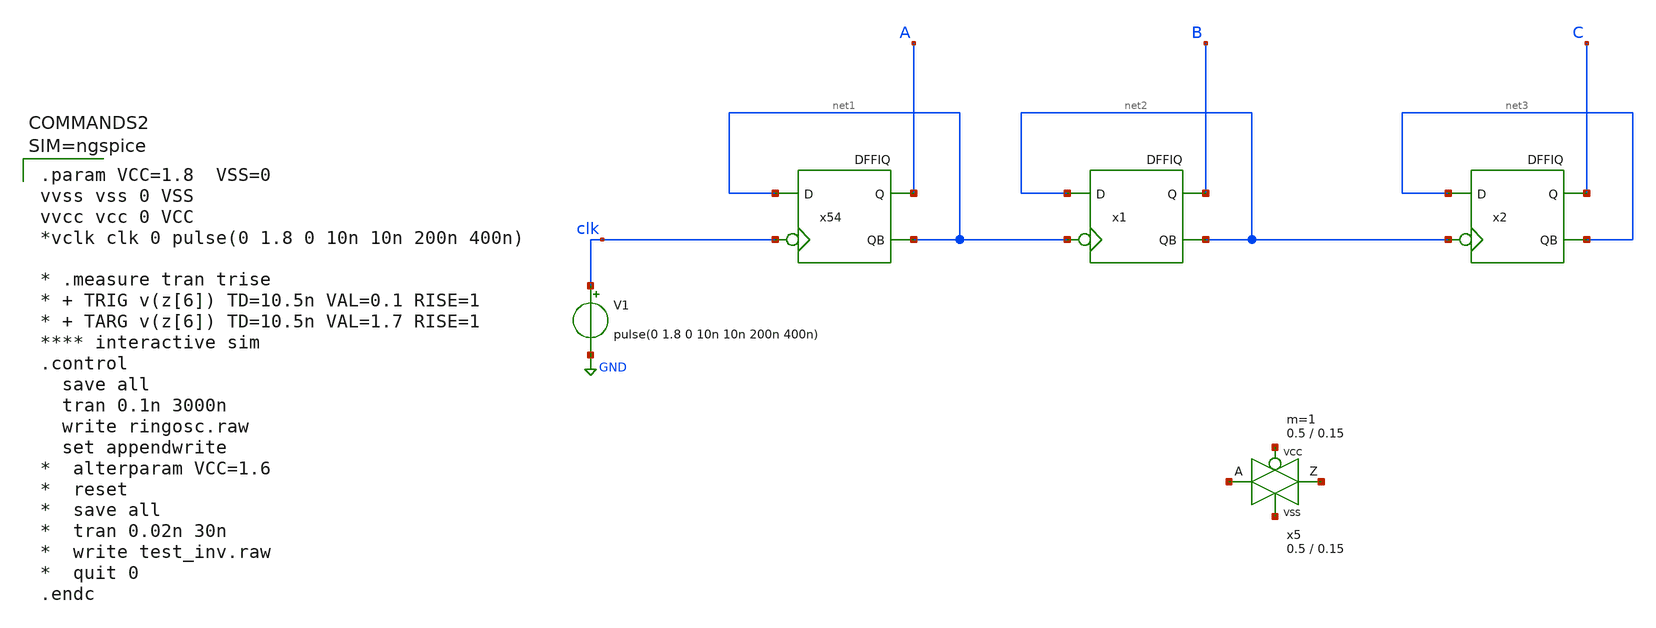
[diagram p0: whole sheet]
** sch_path: xschem/divider.sch
.lib $::SKYWATER_MODELS/sky130.lib.spice tt
.include $::SKYWATER_STDCELLS/sky130_fd_sc_hd.spice

**.subckt divider
x54 A net1 net1 clk VCC VSS VCC VSS DFFIQ
x1 B net2 net2 net1 VCC VSS VCC VSS DFFIQ
x2 C net3 net3 net2 VCC VSS VCC VSS DFFIQ
V1 clk GND pulse(0 1.8 0 10n 10n 200n 400n)
x5 net4 net5 net6 net7 VCC VSS passgate W_N=0.5 L_N=0.15 W_P=0.5 L_P=0.15 m=1
**** begin user architecture code


.param VCC=1.8  VSS=0
vvss vss 0 VSS
vvcc vcc 0 VCC
*vclk clk 0 pulse(0 1.8 0 10n 10n 200n 400n)

* .measure tran trise
* + TRIG v(z[6]) TD=10.5n VAL=0.1 RISE=1
* + TARG v(z[6]) TD=10.5n VAL=1.7 RISE=1
**** interactive sim
.control
  save all
  tran 0.1n 3000n
  write ringosc.raw
  set appendwrite
*  alterparam VCC=1.6
*  reset
*  save all
*  tran 0.02n 30n
*  write test_inv.raw
*  quit 0
.endc



**** end user architecture code
**.ends

* expanding   symbol:  sky130_tests/passgate.sym # of pins=4
** sym_path: sky130_tests/passgate.sym
** sch_path: sky130_tests/passgate.sch
.subckt passgate Z A GP GN VCCBPIN VSSBPIN  W_N=1 L_N=0.2 W_P=1 L_P=0.2

*.iopin A
*.iopin Z
*.ipin GP
*.ipin GN
XM1 A GN Z VSS sky130_fd_pr__nfet_01v8 W=W_N L=L_N ad='W * 0.29' pd='W + 2 * 0.29' as='W * 0.29' ps='W + 2 * 0.29'
+ nrd=0 nrs=0 sa=0 sb=0 sd=0 nf=1 mult=1
XM2 A GP Z VCC sky130_fd_pr__pfet_01v8 W=W_P L=L_P ad='W * 0.29' pd='W + 2 * 0.29' as='W * 0.29' ps='W + 2 * 0.29'
+ nrd=0 nrs=0 sa=0 sb=0 sd=0 nf=1 mult=1
.ends

.GLOBAL GND
.end
